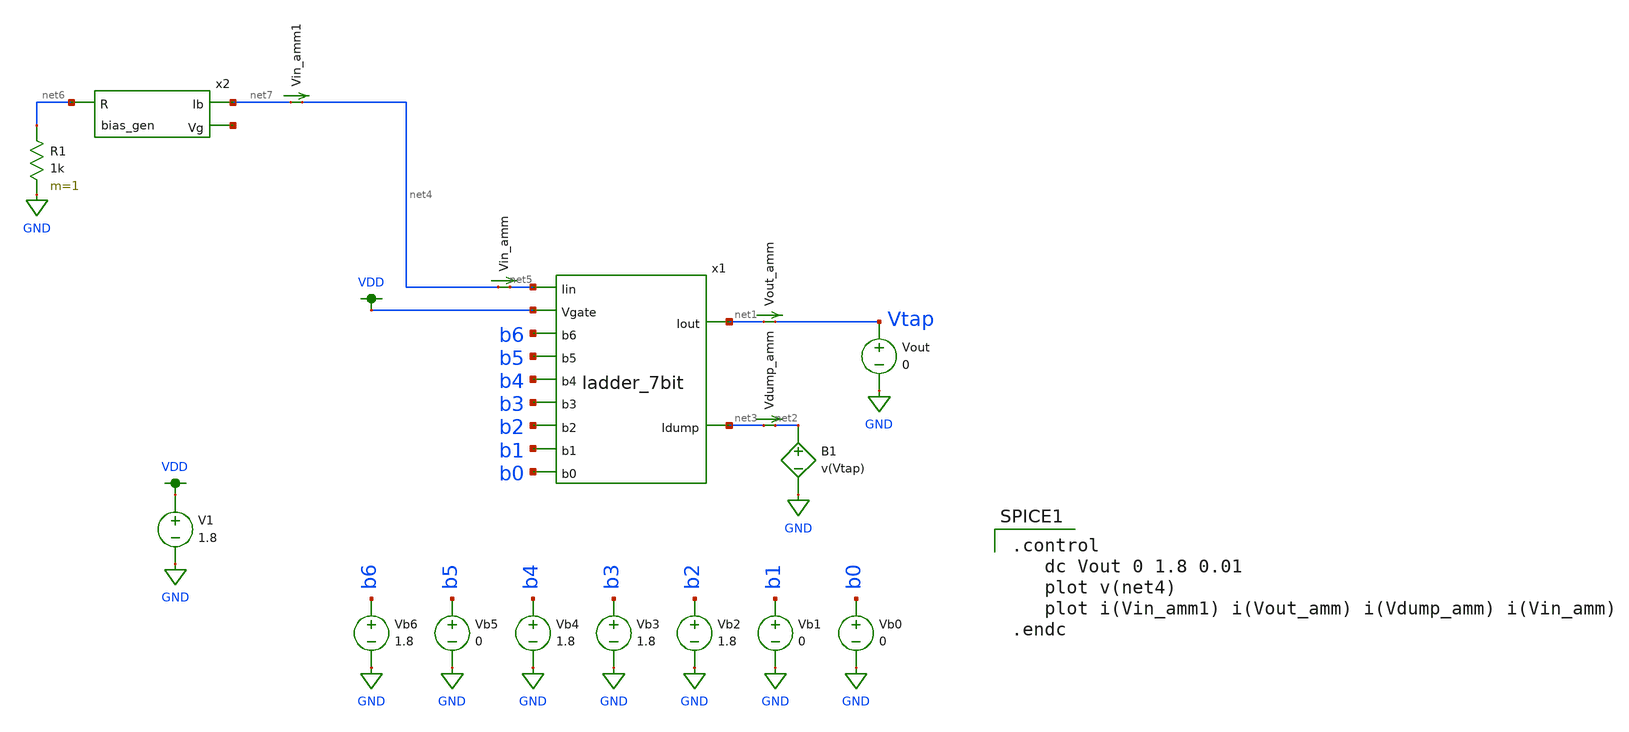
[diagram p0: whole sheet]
** sch_path: test_harness_dcvout.sch
**.subckt test_harness_dcvout
Vb0 b0 GND 0
Vb1 b1 GND 0
Vb2 b2 GND 1.8
Vb3 b3 GND 1.8
Vb4 b4 GND 1.8
Vb5 b5 GND 0
Vb6 b6 GND 1.8
Vout Vtap GND 0
Vout_amm net1 Vtap 0
.save i(vout_amm)
Vdump_amm net3 net2 0
.save i(vdump_amm)
x1 VDD net5 net3 net1 b5 b4 b1 b2 b3 b0 b6 ladder_7bit
Vin_amm net4 net5 0
.save i(vin_amm)
x2 net7 net8 net6 bias_gen
R1 net6 GND 1k m=1
Vin_amm1 net7 net4 0
.save i(vin_amm1)
B1 net2 GND V=v(Vtap)
V1 VDD GND 1.8
**** begin user architecture code

.control
   dc Vout 0 1.8 0.01
   plot v(net4)
   plot i(Vin_amm1) i(Vout_amm) i(Vdump_amm) i(Vin_amm)
.endc


.option wnflag=1
.param MC_SWITCH=0.0
.lib ~/skywater/skywater-pdk/libraries/sky130_fd_pr_ngspice/latest/models/sky130.lib.spice tt

**** end user architecture code
**.ends

* expanding   symbol:  ./ladder_7bit.sym # of pins=11
** sym_path: ladder_7bit.sym
** sch_path: ladder_7bit.sch
.subckt ladder_7bit Vgate Iin Idump Iout b5 b4 b1 b2 b3 b0 b6
*.opin Idump
*.opin Iout
*.ipin Vgate
*.ipin Iin
*.ipin b6
*.ipin b5
*.ipin b4
*.ipin b3
*.ipin b2
*.ipin b1
*.ipin b0
x1 Iin net8 Vgate Idump Iout net1 b6 ladder_1bit
x2 net8 net9 Vgate Idump Iout net2 b5 ladder_1bit
x3 net9 net10 Vgate Idump Iout net3 b4 ladder_1bit
x4 net10 net11 Vgate Idump Iout net4 b3 ladder_1bit
x5 net11 net12 Vgate Idump Iout net5 b2 ladder_1bit
x6 net12 net13 Vgate Idump Iout net6 b1 ladder_1bit
x7 net13 net14 Vgate Idump Iout net7 b0 ladder_1bit
XM1 Idump Vgate net14 GND sky130_fd_pr__nfet_01v8 L=0.15 W=1 nf=1 ad='int((nf+1)/2) * W/nf * 0.29' as='int((nf+2)/2) * W/nf * 0.29'
+ pd='2*int((nf+1)/2) * (W/nf + 0.29)' ps='2*int((nf+2)/2) * (W/nf + 0.29)' nrd='0.29 / W' nrs='0.29 / W'
+ sa=0 sb=0 sd=0 mult=1 m=1
X8 b6 net15 VDD GND inverter
X9 b5 net16 VDD GND inverter
X10 b4 net17 VDD GND inverter
X11 b3 net18 VDD GND inverter
X12 b2 net19 VDD GND inverter
X13 b1 net20 VDD GND inverter
X14 b0 net21 VDD GND inverter
.ends


* expanding   symbol:  ./bias_gen.sym # of pins=3
** sym_path: bias_gen.sym
** sch_path: bias_gen.sch
.subckt bias_gen Ib Vg R
*.ipin R
*.opin Ib
*.opin Vg
XM2 R net2 net2 GND sky130_fd_pr__nfet_01v8 L=0.5 W=96 nf=1 ad='int((nf+1)/2) * W/nf * 0.29' as='int((nf+2)/2) * W/nf * 0.29'
+ pd='2*int((nf+1)/2) * (W/nf + 0.29)' ps='2*int((nf+2)/2) * (W/nf + 0.29)' nrd='0.29 / W' nrs='0.29 / W'
+ sa=0 sb=0 sd=0 mult=1 m=1
XM3 VDD net1 net1 VDD sky130_fd_pr__pfet_01v8 L=0.5 W=12 nf=1 ad='int((nf+1)/2) * W/nf * 0.29' as='int((nf+2)/2) * W/nf * 0.29'
+ pd='2*int((nf+1)/2) * (W/nf + 0.29)' ps='2*int((nf+2)/2) * (W/nf + 0.29)' nrd='0.29 / W' nrs='0.29 / W'
+ sa=0 sb=0 sd=0 mult=1 m=1
XM1 VDD Vg net2 VDD sky130_fd_pr__pfet_01v8 L=0.5 W=12 nf=1 ad='int((nf+1)/2) * W/nf * 0.29' as='int((nf+2)/2) * W/nf * 0.29'
+ pd='2*int((nf+1)/2) * (W/nf + 0.29)' ps='2*int((nf+2)/2) * (W/nf + 0.29)' nrd='0.29 / W' nrs='0.29 / W'
+ sa=0 sb=0 sd=0 mult=1 m=1
XM4 Vg net1 VDD VDD sky130_fd_pr__pfet_01v8 L=0.5 W=12 nf=1 ad='int((nf+1)/2) * W/nf * 0.29' as='int((nf+2)/2) * W/nf * 0.29'
+ pd='2*int((nf+1)/2) * (W/nf + 0.29)' ps='2*int((nf+2)/2) * (W/nf + 0.29)' nrd='0.29 / W' nrs='0.29 / W'
+ sa=0 sb=0 sd=0 mult=1 m=1
XM5 net3 Vg VDD VDD sky130_fd_pr__pfet_01v8 L=0.5 W=12 nf=1 ad='int((nf+1)/2) * W/nf * 0.29' as='int((nf+2)/2) * W/nf * 0.29'
+ pd='2*int((nf+1)/2) * (W/nf + 0.29)' ps='2*int((nf+2)/2) * (W/nf + 0.29)' nrd='0.29 / W' nrs='0.29 / W'
+ sa=0 sb=0 sd=0 mult=1 m=1
XM7 Ib Vg VDD VDD sky130_fd_pr__pfet_01v8 L=0.5 W=12 nf=1 ad='int((nf+1)/2) * W/nf * 0.29' as='int((nf+2)/2) * W/nf * 0.29'
+ pd='2*int((nf+1)/2) * (W/nf + 0.29)' ps='2*int((nf+2)/2) * (W/nf + 0.29)' nrd='0.29 / W' nrs='0.29 / W'
+ sa=0 sb=0 sd=0 mult=1 m=1
XM6 net1 net2 GND GND sky130_fd_pr__nfet_01v8 L=0.5 W=12 nf=1 ad='int((nf+1)/2) * W/nf * 0.29' as='int((nf+2)/2) * W/nf * 0.29'
+ pd='2*int((nf+1)/2) * (W/nf + 0.29)' ps='2*int((nf+2)/2) * (W/nf + 0.29)' nrd='0.29 / W' nrs='0.29 / W'
+ sa=0 sb=0 sd=0 mult=1 m=1
XM8 GND net3 Vg GND sky130_fd_pr__nfet_01v8 L=0.5 W=12 nf=1 ad='int((nf+1)/2) * W/nf * 0.29' as='int((nf+2)/2) * W/nf * 0.29'
+ pd='2*int((nf+1)/2) * (W/nf + 0.29)' ps='2*int((nf+2)/2) * (W/nf + 0.29)' nrd='0.29 / W' nrs='0.29 / W'
+ sa=0 sb=0 sd=0 mult=1 m=1
XM9 net3 net3 GND GND sky130_fd_pr__nfet_01v8 L=0.5 W=12 nf=1 ad='int((nf+1)/2) * W/nf * 0.29' as='int((nf+2)/2) * W/nf * 0.29'
+ pd='2*int((nf+1)/2) * (W/nf + 0.29)' ps='2*int((nf+2)/2) * (W/nf + 0.29)' nrd='0.29 / W' nrs='0.29 / W'
+ sa=0 sb=0 sd=0 mult=1 m=1
.ends


* expanding   symbol:  /home/madvlsi/R2R-DAC/ladder_1bit.sym # of pins=7
** sym_path: ladder_1bit.sym
** sch_path: ladder_1bit.sch
.subckt ladder_1bit Iin_in Iin_out Vg I_dump Iout B_bar B
*.ipin Iin_in
*.ipin Vg
*.ipin B
*.ipin B_bar
*.opin Iin_out
*.opin I_dump
*.opin Iout
XM5 net1 Vg Iin_in GND sky130_fd_pr__nfet_01v8 L=0.15 W=1 nf=1 ad='int((nf+1)/2) * W/nf * 0.29' as='int((nf+2)/2) * W/nf * 0.29'
+ pd='2*int((nf+1)/2) * (W/nf + 0.29)' ps='2*int((nf+2)/2) * (W/nf + 0.29)' nrd='0.29 / W' nrs='0.29 / W'
+ sa=0 sb=0 sd=0 mult=1 m=1
XM6 Iout B net1 GND sky130_fd_pr__nfet_01v8 L=0.15 W=1 nf=1 ad='int((nf+1)/2) * W/nf * 0.29' as='int((nf+2)/2) * W/nf * 0.29'
+ pd='2*int((nf+1)/2) * (W/nf + 0.29)' ps='2*int((nf+2)/2) * (W/nf + 0.29)' nrd='0.29 / W' nrs='0.29 / W'
+ sa=0 sb=0 sd=0 mult=1 m=1
XM7 net1 B_bar I_dump GND sky130_fd_pr__nfet_01v8 L=0.15 W=1 nf=1 ad='int((nf+1)/2) * W/nf * 0.29' as='int((nf+2)/2) * W/nf * 0.29'
+ pd='2*int((nf+1)/2) * (W/nf + 0.29)' ps='2*int((nf+2)/2) * (W/nf + 0.29)' nrd='0.29 / W' nrs='0.29 / W'
+ sa=0 sb=0 sd=0 mult=1 m=1
XM8 Iin_in Vg Iin_out GND sky130_fd_pr__nfet_01v8 L=0.15 W=1 nf=1 ad='int((nf+1)/2) * W/nf * 0.29' as='int((nf+2)/2) * W/nf * 0.29'
+ pd='2*int((nf+1)/2) * (W/nf + 0.29)' ps='2*int((nf+2)/2) * (W/nf + 0.29)' nrd='0.29 / W' nrs='0.29 / W'
+ sa=0 sb=0 sd=0 mult=1 m=1
.ends


* expanding   symbol:  /home/madvlsi/Documents/mp1/inverter.sym # of pins=4
** sym_path: /home/madvlsi/Documents/mp1/inverter.sym
** sch_path: /home/madvlsi/Documents/mp1/inverter.sch
.subckt inverter A Y VP VN
*.ipin A
*.iopin VP
*.iopin VN
*.opin Y
XM3 Y A VP VP sky130_fd_pr__pfet_01v8 L=0.15 W=1 nf=1 ad='int((nf+1)/2) * W/nf * 0.29' as='int((nf+2)/2) * W/nf * 0.29'
+ pd='2*int((nf+1)/2) * (W/nf + 0.29)' ps='2*int((nf+2)/2) * (W/nf + 0.29)' nrd='0.29 / W' nrs='0.29 / W'
+ sa=0 sb=0 sd=0 mult=1 m=1
XM4 Y A VN VN sky130_fd_pr__nfet_01v8 L=0.15 W=1 nf=1 ad='int((nf+1)/2) * W/nf * 0.29' as='int((nf+2)/2) * W/nf * 0.29'
+ pd='2*int((nf+1)/2) * (W/nf + 0.29)' ps='2*int((nf+2)/2) * (W/nf + 0.29)' nrd='0.29 / W' nrs='0.29 / W'
+ sa=0 sb=0 sd=0 mult=1 m=1
.ends

.GLOBAL GND
.GLOBAL VDD
.end
